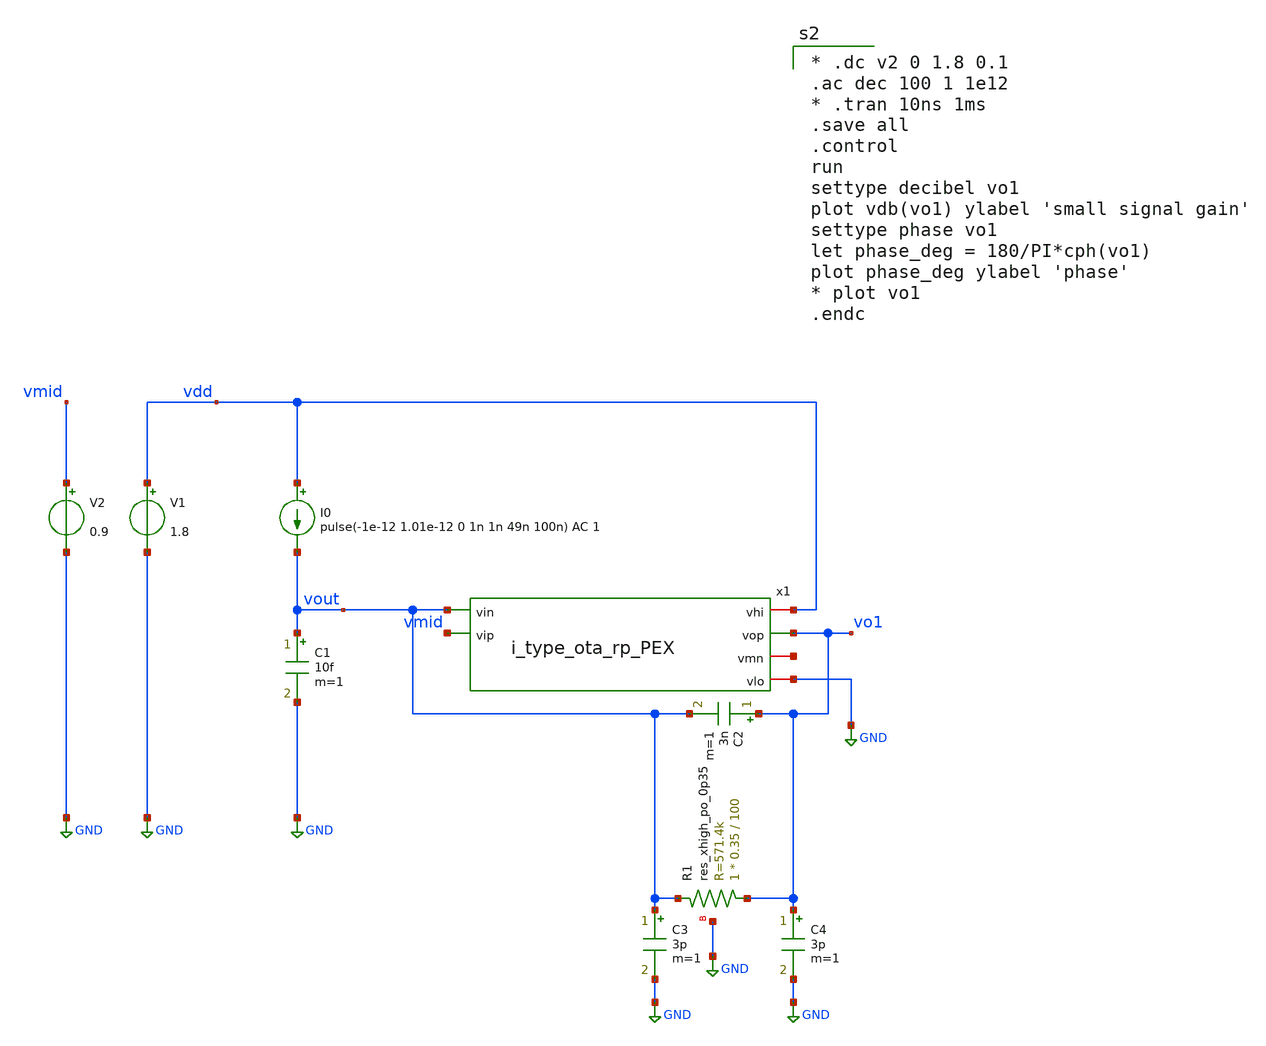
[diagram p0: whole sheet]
** sch_path: xschem/idetect_test.sch
**.subckt idetect_test
I0 vdd vout pulse(-1e-12 1.01e-12 0 1n 1n 49n 100n) AC 1
V1 vdd GND 1.8
C1 vout GND 10f m=1
V2 vmid GND 0.9
XR1 vo1 vout GND sky130_fd_pr__res_xhigh_po_0p35 L=100 mult=1 m=1
C2 vo1 vout 3n m=1
x1 vdd vo1 vout vmid net1 GND i_type_ota_rp_PEX
C3 vout GND 3p m=1
C4 vo1 GND 3p m=1
**** begin user architecture code
.lib $::SKYWATER_MODELS/sky130.lib.spice tt
.include $::PDKPATH/libs.ref/sky130_fd_sc_hs/spice/sky130_fd_sc_hs.spice


* .dc v2 0 1.8 0.1
.ac dec 100 1 1e12
* .tran 10ns 1ms
.save all
.control
run
settype decibel vo1
plot vdb(vo1) ylabel 'small signal gain'
settype phase vo1
let phase_deg = 180/PI*cph(vo1)
plot phase_deg ylabel 'phase'
* plot vo1
.endc


**** end user architecture code
**.ends

* expanding   symbol:  i_type_ota_rp_PEX.sym # of pins=6
** sym_path: xschem/i_type_ota_rp_PEX.sym
** sch_path: xschem/i_type_ota_rp_PEX.sch
.subckt i_type_ota_rp_PEX vhi vop vin vip vmn vlo
*.ipin vip
*.ipin vin
*.opin vop
*.iopin vhi
*.iopin vlo
*.iopin vmn
XM6 net1 net1 vlo vlo sky130_fd_pr__nfet_01v8 L=2 W=5 nf=1 ad='int((nf+1)/2) * W/nf * 0.29' as='int((nf+2)/2) * W/nf * 0.29'
+ pd='2*int((nf+1)/2) * (W/nf + 0.29)' ps='2*int((nf+2)/2) * (W/nf + 0.29)' nrd='0.29 / W' nrs='0.29 / W'
+ sa=0 sb=0 sd=0 mult=1 m=1
I1 vhi net1 10u
**** begin user architecture code

* NGSPICE file created from cmota_1_flat.ext - technology: sky130A

.subckt cmota_1_flat VHI VLO VREF VIP VIN VOP VMN

X0 VMN li_5300_n960# VLO sky130_fd_pr__res_high_po w=690000u l=5.83e+06u
X1 VHI DN VMN VHI sky130_fd_pr__pfet_01v8 ad=0p pd=0u as=0p ps=0u w=1e+07u l=300000u
X2 VHI DN DN VHI sky130_fd_pr__pfet_01v8 ad=0p pd=0u as=0p ps=0u w=1e+07u l=300000u
X3 VHI DP VOP VHI sky130_fd_pr__pfet_01v8 ad=0p pd=0u as=0p ps=0u w=1e+07u l=300000u
X4 DN VIN COM VLO sky130_fd_pr__nfet_01v8_lvt ad=0p pd=0u as=0p ps=0u w=2.5e+06u l=150000u
X5 COM VIN DN VLO sky130_fd_pr__nfet_01v8_lvt ad=0p pd=0u as=0p ps=0u w=2.5e+06u l=150000u
X6 DP VIP COM VLO sky130_fd_pr__nfet_01v8_lvt ad=0p pd=0u as=0p ps=0u w=2.5e+06u l=150000u
X7 VMN DN VHI VHI sky130_fd_pr__pfet_01v8 ad=0p pd=0u as=0p ps=0u w=1e+07u l=300000u
X8 VMN DN VHI VHI sky130_fd_pr__pfet_01v8 ad=0p pd=0u as=0p ps=0u w=1e+07u l=300000u
X9 VHI VHI VOP VHI sky130_fd_pr__pfet_01v8 ad=0p pd=0u as=0p ps=0u w=1e+07u l=300000u
X10 a_2925_285# DN VHI VHI sky130_fd_pr__pfet_01v8 ad=0p pd=0u as=0p ps=0u w=1e+07u l=300000u
X11 DP VIP COM VLO sky130_fd_pr__nfet_01v8_lvt ad=0p pd=0u as=0p ps=0u w=2.5e+06u l=150000u
X12 li_5300_n960# VOP sky130_fd_pr__cap_mim_m3_2 l=1.32e+07u w=3.7e+06u
X13 VOP DP VHI VHI sky130_fd_pr__pfet_01v8 ad=0p pd=0u as=0p ps=0u w=1e+07u l=300000u
X14 VOP DP VHI VHI sky130_fd_pr__pfet_01v8 ad=0p pd=0u as=0p ps=0u w=1e+07u l=300000u
X15 VOP DP VHI VHI sky130_fd_pr__pfet_01v8 ad=0p pd=0u as=0p ps=0u w=1e+07u l=300000u
X16 COM VLO VLO VLO sky130_fd_pr__nfet_01v8_lvt ad=0p pd=0u as=0p ps=0u w=2.5e+06u l=150000u
X17 VLO VMN VOP VLO sky130_fd_pr__nfet_01v8 ad=0p pd=0u as=0p ps=0u w=1e+07u l=300000u
X18 VHI DN VMN VHI sky130_fd_pr__pfet_01v8 ad=0p pd=0u as=0p ps=0u w=1e+07u l=300000u
X19 VLO VLO VLO VLO sky130_fd_pr__nfet_01v8 ad=0p pd=0u as=0p ps=0u w=1e+07u l=300000u
X20 VHI DN DP VHI sky130_fd_pr__pfet_01v8 ad=0p pd=0u as=0p ps=0u w=1e+07u l=300000u
X21 VHI DP DP VHI sky130_fd_pr__pfet_01v8 ad=0p pd=0u as=0p ps=0u w=1e+07u l=300000u
X22 COM VIP DP VLO sky130_fd_pr__nfet_01v8_lvt ad=0p pd=0u as=0p ps=0u w=2.5e+06u l=150000u
X23 VLO VREF COM VLO sky130_fd_pr__nfet_01v8 ad=0p pd=0u as=0p ps=0u w=1e+07u l=2e+06u
X24 VMN VHI VHI VHI sky130_fd_pr__pfet_01v8 ad=0p pd=0u as=0p ps=0u w=1e+07u l=300000u
X25 DN DN VHI VHI sky130_fd_pr__pfet_01v8 ad=0p pd=0u as=0p ps=0u w=1e+07u l=300000u
X26 VHI DP VOP VHI sky130_fd_pr__pfet_01v8 ad=0p pd=0u as=0p ps=0u w=1e+07u l=300000u
X27 VLO VLO VLO VLO sky130_fd_pr__nfet_01v8_lvt ad=0p pd=0u as=0p ps=0u w=2.5e+06u l=150000u
X28 VLO VREF COM VLO sky130_fd_pr__nfet_01v8 ad=0p pd=0u as=0p ps=0u w=1e+07u l=2e+06u
X29 COM VIN DN VLO sky130_fd_pr__nfet_01v8_lvt ad=0p pd=0u as=0p ps=0u w=2.5e+06u l=150000u
X30 DN DN VHI VHI sky130_fd_pr__pfet_01v8 ad=0p pd=0u as=0p ps=0u w=1e+07u l=300000u
X31 DP DN VHI VHI sky130_fd_pr__pfet_01v8 ad=0p pd=0u as=0p ps=0u w=1e+07u l=300000u
X32 DN DP VHI VHI sky130_fd_pr__pfet_01v8 ad=0p pd=0u as=0p ps=0u w=1e+07u l=300000u
X33 DP DP VHI VHI sky130_fd_pr__pfet_01v8 ad=0p pd=0u as=0p ps=0u w=1e+07u l=300000u
X34 DN VIN COM VLO sky130_fd_pr__nfet_01v8_lvt ad=0p pd=0u as=0p ps=0u w=2.5e+06u l=150000u
X35 VLO VLO VLO VLO sky130_fd_pr__nfet_01v8 ad=0p pd=0u as=0p ps=0u w=1e+07u l=300000u
X36 COM VIP DP VLO sky130_fd_pr__nfet_01v8_lvt ad=0p pd=0u as=0p ps=0u w=2.5e+06u l=150000u
X37 VHI DN DN VHI sky130_fd_pr__pfet_01v8 ad=0p pd=0u as=0p ps=0u w=1e+07u l=300000u
X38 VOP DP VHI VHI sky130_fd_pr__pfet_01v8 ad=0p pd=0u as=0p ps=0u w=1e+07u l=300000u
X39 VMN VMN VLO VLO sky130_fd_pr__nfet_01v8 ad=0p pd=0u as=0p ps=0u w=1e+07u l=300000u
X40 VLO VMN VMN VLO sky130_fd_pr__nfet_01v8 ad=0p pd=0u as=0p ps=0u w=1e+07u l=300000u
X41 VLO VLO VLO VLO sky130_fd_pr__nfet_01v8 ad=0p pd=0u as=0p ps=0u w=1e+07u l=300000u
X42 VOP VMN VLO VLO sky130_fd_pr__nfet_01v8 ad=0p pd=0u as=0p ps=0u w=1e+07u l=300000u
X43 VHI DP DN VHI sky130_fd_pr__pfet_01v8 ad=0p pd=0u as=0p ps=0u w=1e+07u l=300000u
X44 VLO VMN VOP VLO sky130_fd_pr__nfet_01v8 ad=0p pd=0u as=0p ps=0u w=1e+07u l=300000u
X45 VHI DN VMN VHI sky130_fd_pr__pfet_01v8 ad=0p pd=0u as=0p ps=0u w=1e+07u l=300000u
X46 VLO VLO COM VLO sky130_fd_pr__nfet_01v8_lvt ad=0p pd=0u as=0p ps=0u w=2.5e+06u l=150000u
X47 DN VIN COM VLO sky130_fd_pr__nfet_01v8_lvt ad=0p pd=0u as=0p ps=0u w=2.5e+06u l=150000u
X48 VHI DP a_2217_285# VHI sky130_fd_pr__pfet_01v8 ad=0p pd=0u as=0p ps=0u w=1e+07u l=300000u
X49 VHI DP DP VHI sky130_fd_pr__pfet_01v8 ad=0p pd=0u as=0p ps=0u w=1e+07u l=300000u
X50 VLO VLO VLO VLO sky130_fd_pr__nfet_01v8 ad=0p pd=0u as=0p ps=0u w=1e+07u l=300000u
X51 COM VREF VLO VLO sky130_fd_pr__nfet_01v8 ad=0p pd=0u as=0p ps=0u w=1e+07u l=2e+06u
X52 VLO VLO VLO VLO sky130_fd_pr__nfet_01v8_lvt ad=0p pd=0u as=0p ps=0u w=2.5e+06u l=150000u
X53 COM VIN DN VLO sky130_fd_pr__nfet_01v8_lvt ad=0p pd=0u as=0p ps=0u w=2.5e+06u l=150000u
X54 COM VREF VLO VLO sky130_fd_pr__nfet_01v8 ad=0p pd=0u as=0p ps=0u w=1e+07u l=2e+06u
X55 DP VIP COM VLO sky130_fd_pr__nfet_01v8_lvt ad=0p pd=0u as=0p ps=0u w=2.5e+06u l=150000u
X56 COM VIN DN VLO sky130_fd_pr__nfet_01v8_lvt ad=0p pd=0u as=0p ps=0u w=2.5e+06u l=150000u
X57 VMN DN VHI VHI sky130_fd_pr__pfet_01v8 ad=0p pd=0u as=0p ps=0u w=1e+07u l=300000u
X58 DP DP VHI VHI sky130_fd_pr__pfet_01v8 ad=0p pd=0u as=0p ps=0u w=1e+07u l=300000u
X59 DP VIP COM VLO sky130_fd_pr__nfet_01v8_lvt ad=0p pd=0u as=0p ps=0u w=2.5e+06u l=150000u
X60 a_2217_285# DP VHI VHI sky130_fd_pr__pfet_01v8 ad=0p pd=0u as=0p ps=0u w=1e+07u l=300000u
X61 VMN VMN VLO VLO sky130_fd_pr__nfet_01v8 ad=0p pd=0u as=0p ps=0u w=1e+07u l=300000u
X62 COM VIP DP VLO sky130_fd_pr__nfet_01v8_lvt ad=0p pd=0u as=0p ps=0u w=2.5e+06u l=150000u
X63 VLO VMN VMN VLO sky130_fd_pr__nfet_01v8 ad=0p pd=0u as=0p ps=0u w=1e+07u l=300000u
X64 VOP VMN VLO VLO sky130_fd_pr__nfet_01v8 ad=0p pd=0u as=0p ps=0u w=1e+07u l=300000u
X65 COM VIP DP VLO sky130_fd_pr__nfet_01v8_lvt ad=0p pd=0u as=0p ps=0u w=2.5e+06u l=150000u
X66 VHI DN VMN VHI sky130_fd_pr__pfet_01v8 ad=0p pd=0u as=0p ps=0u w=1e+07u l=300000u
X67 DN VIN COM VLO sky130_fd_pr__nfet_01v8_lvt ad=0p pd=0u as=0p ps=0u w=2.5e+06u l=150000u
X68 VOP li_5300_n960# sky130_fd_pr__cap_mim_m3_1 l=1.32e+07u w=3.7e+06u
X69 VHI DN a_2925_285# VHI sky130_fd_pr__pfet_01v8 ad=0p pd=0u as=0p ps=0u w=1e+07u l=300000u
X70 VHI DP VOP VHI sky130_fd_pr__pfet_01v8 ad=0p pd=0u as=0p ps=0u w=1e+07u l=300000u
C0 li_5300_n960# VHI 2.02fF
C1 VMN VHI 17.75fF
C2 li_5300_n960# VOP 9.33fF
C3 VHI a_2217_285# 4.31fF
C4 COM DP 6.02fF
C5 VHI DP 16.22fF
C6 COM VREF 2.35fF
C7 COM DN 6.05fF
C8 VHI DN 16.22fF
C9 VOP VHI 18.23fF
C10 a_2925_285# VHI 4.31fF
C11 VREF VLO 7.20fF $ **FLOATING
C12 COM VLO 6.11fF $ **FLOATING
C13 VOP VLO 9.34fF $ **FLOATING
C14 VHI VLO 35.14fF $ **FLOATING
C15 li_5300_n960# VLO 3.02fF $ **FLOATING
C16 VMN VLO 13.45fF $ **FLOATING


.ends


XDUT vhi vlo vref vip vin vop vmn cmota_1_flat


**** end user architecture code
XR1 vref net1 vlo sky130_fd_pr__res_high_po_0p35 L=0.35 mult=1 m=1
C1 vref vlo 1p m=1
.ends

.GLOBAL GND
.end
